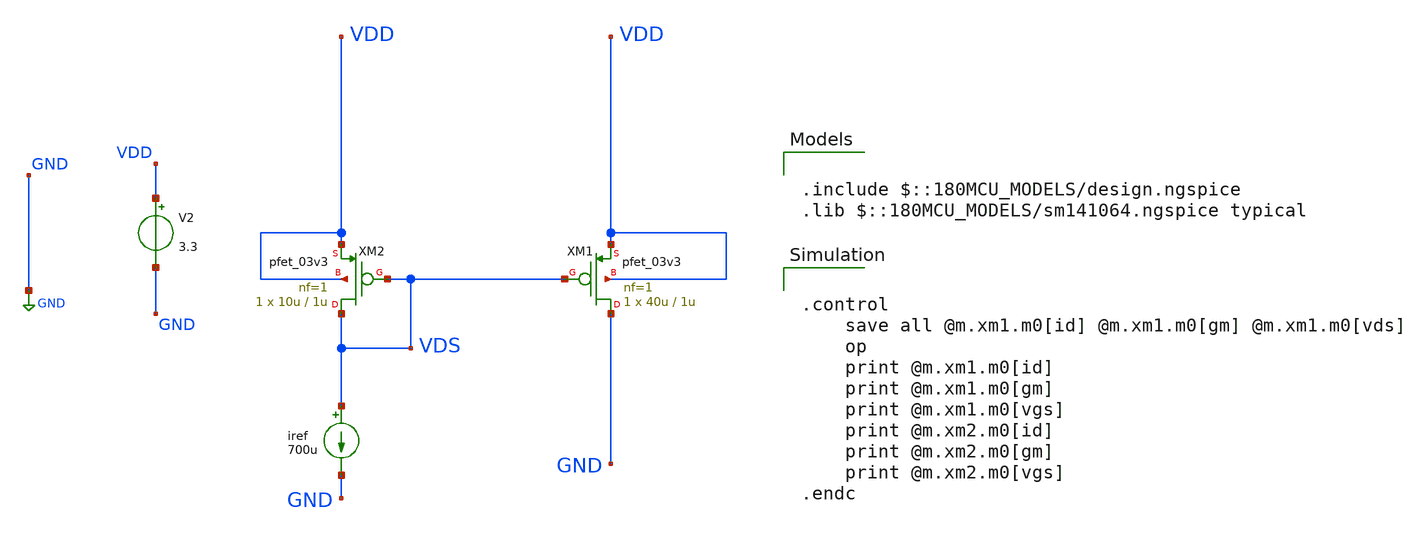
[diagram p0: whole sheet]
** sch_path: designs/libs/session_2/current_mirror_pmos.sch
**.subckt current_mirror_pmos
iref VDS GND 700u
V2 VDD GND 3.3
XM1 GND VDS VDD VDD pfet_03v3 L=1u W=40u nf=1 ad='int((nf+1)/2) * W/nf * 0.18u' as='int((nf+2)/2) * W/nf * 0.18u'
+ pd='2*int((nf+1)/2) * (W/nf + 0.18u)' ps='2*int((nf+2)/2) * (W/nf + 0.18u)' nrd='0.18u / W' nrs='0.18u / W'
+ sa=0 sb=0 sd=0 m=1
XM2 VDS VDS VDD VDD pfet_03v3 L=1u W=10u nf=1 ad='int((nf+1)/2) * W/nf * 0.18u' as='int((nf+2)/2) * W/nf * 0.18u'
+ pd='2*int((nf+1)/2) * (W/nf + 0.18u)' ps='2*int((nf+2)/2) * (W/nf + 0.18u)' nrd='0.18u / W' nrs='0.18u / W'
+ sa=0 sb=0 sd=0 m=1
**** begin user architecture code

.include $::180MCU_MODELS/design.ngspice
.lib $::180MCU_MODELS/sm141064.ngspice typical



.control
    save all @m.xm1.m0[id] @m.xm1.m0[gm] @m.xm1.m0[vds]
    op
    print @m.xm1.m0[id]
    print @m.xm1.m0[gm]
    print @m.xm1.m0[vgs]
    print @m.xm2.m0[id]
    print @m.xm2.m0[gm]
    print @m.xm2.m0[vgs]
.endc


**** end user architecture code
**.ends
.GLOBAL GND
.end
